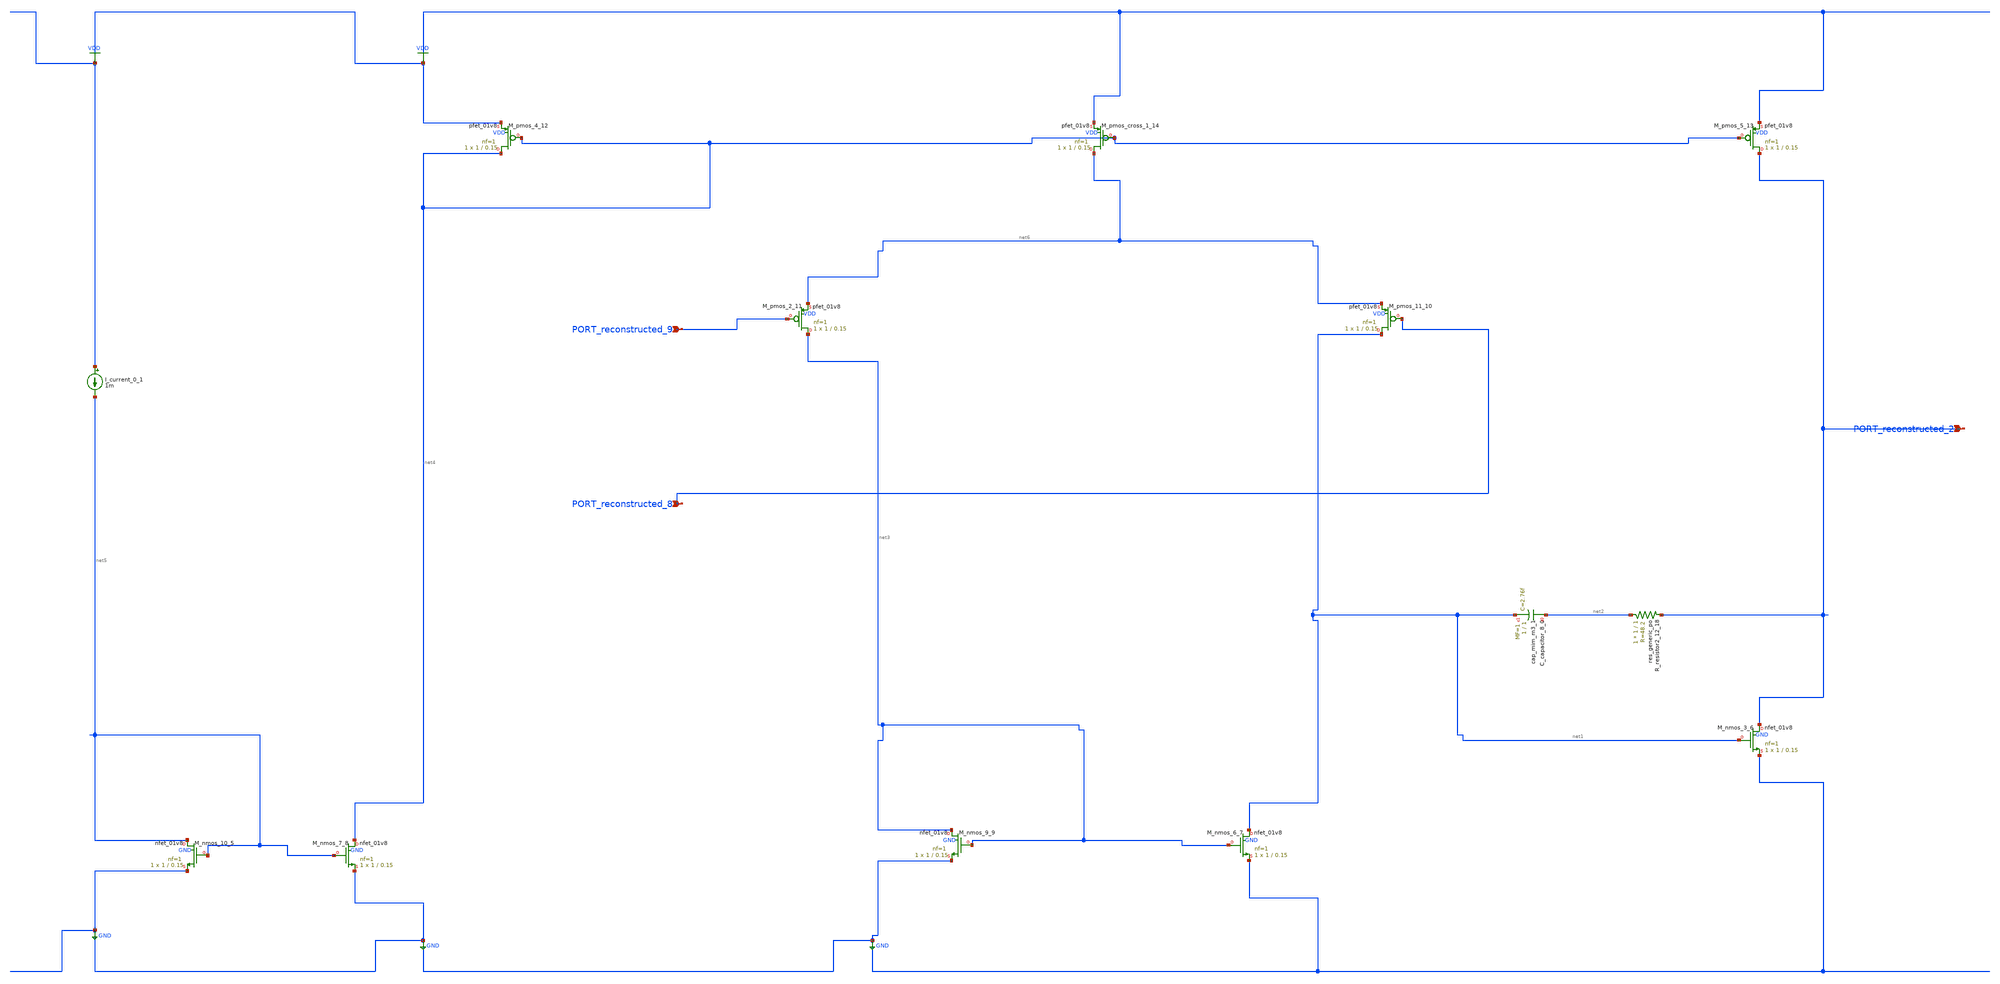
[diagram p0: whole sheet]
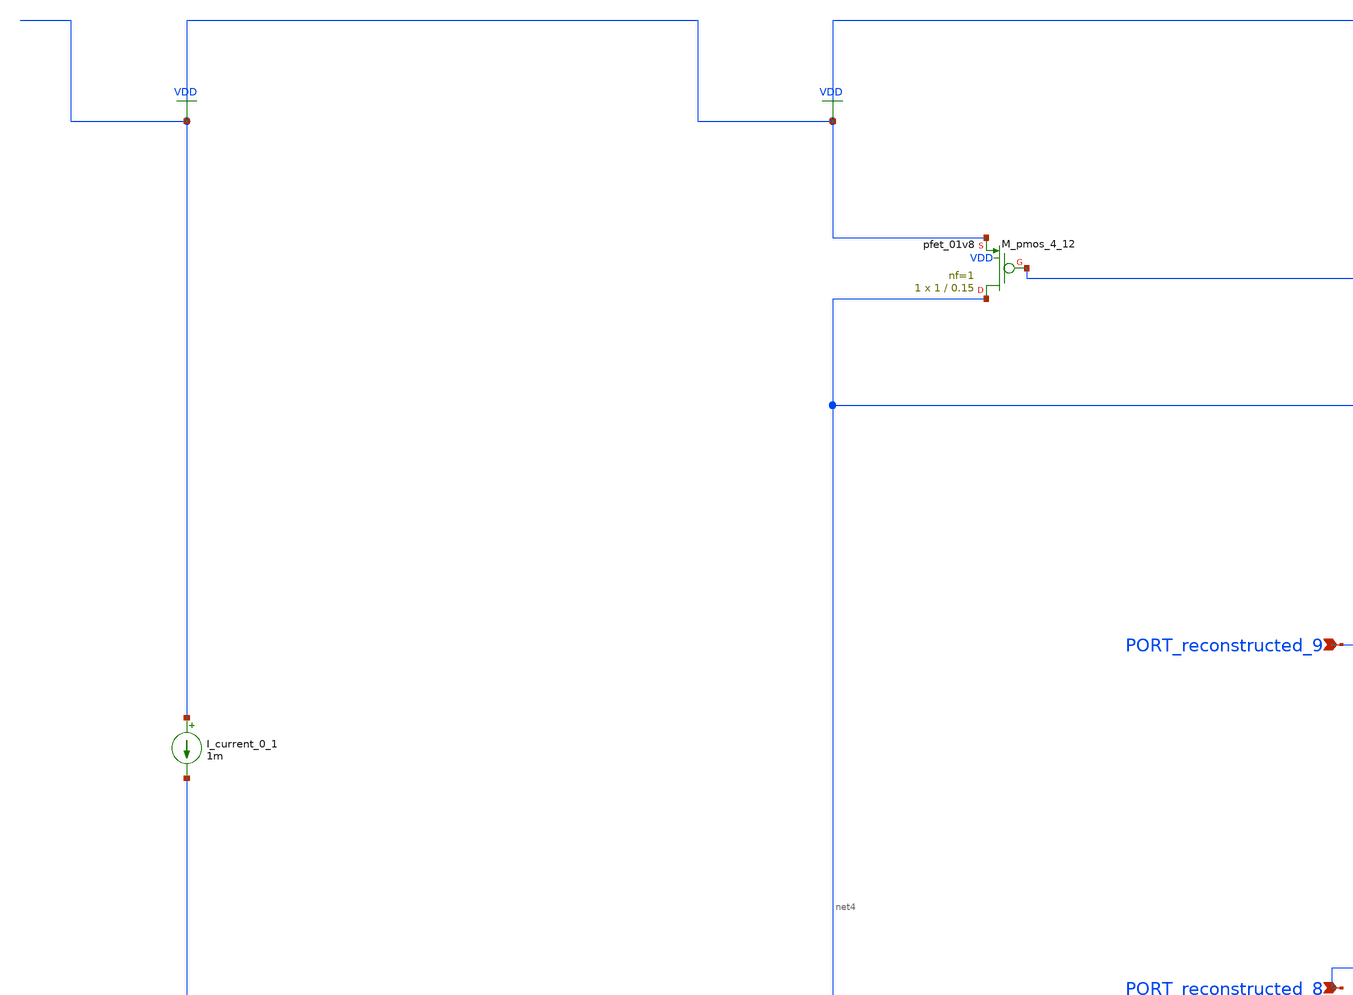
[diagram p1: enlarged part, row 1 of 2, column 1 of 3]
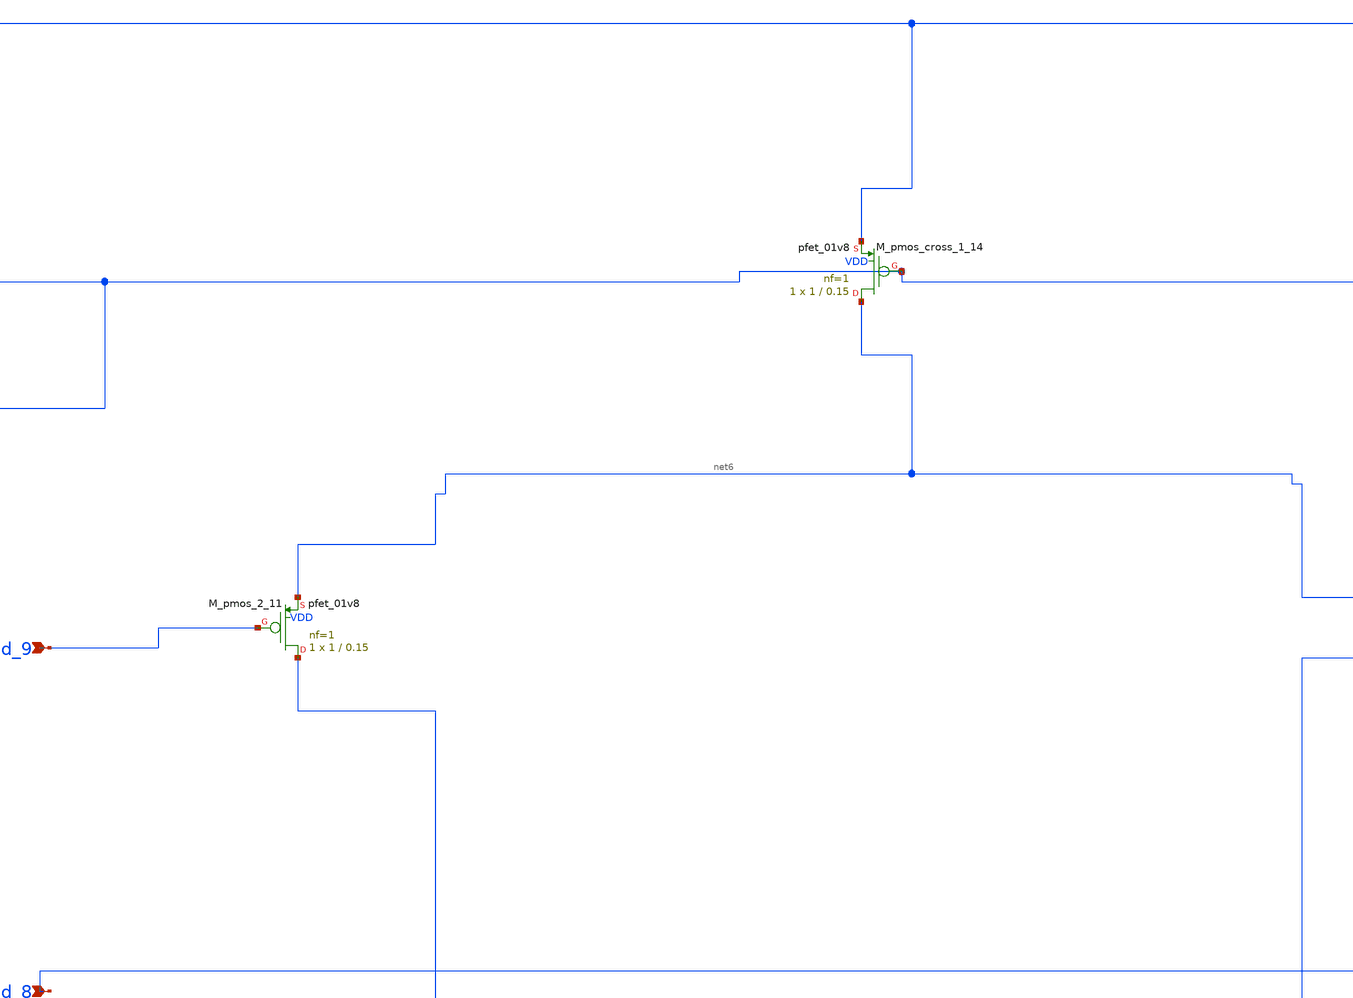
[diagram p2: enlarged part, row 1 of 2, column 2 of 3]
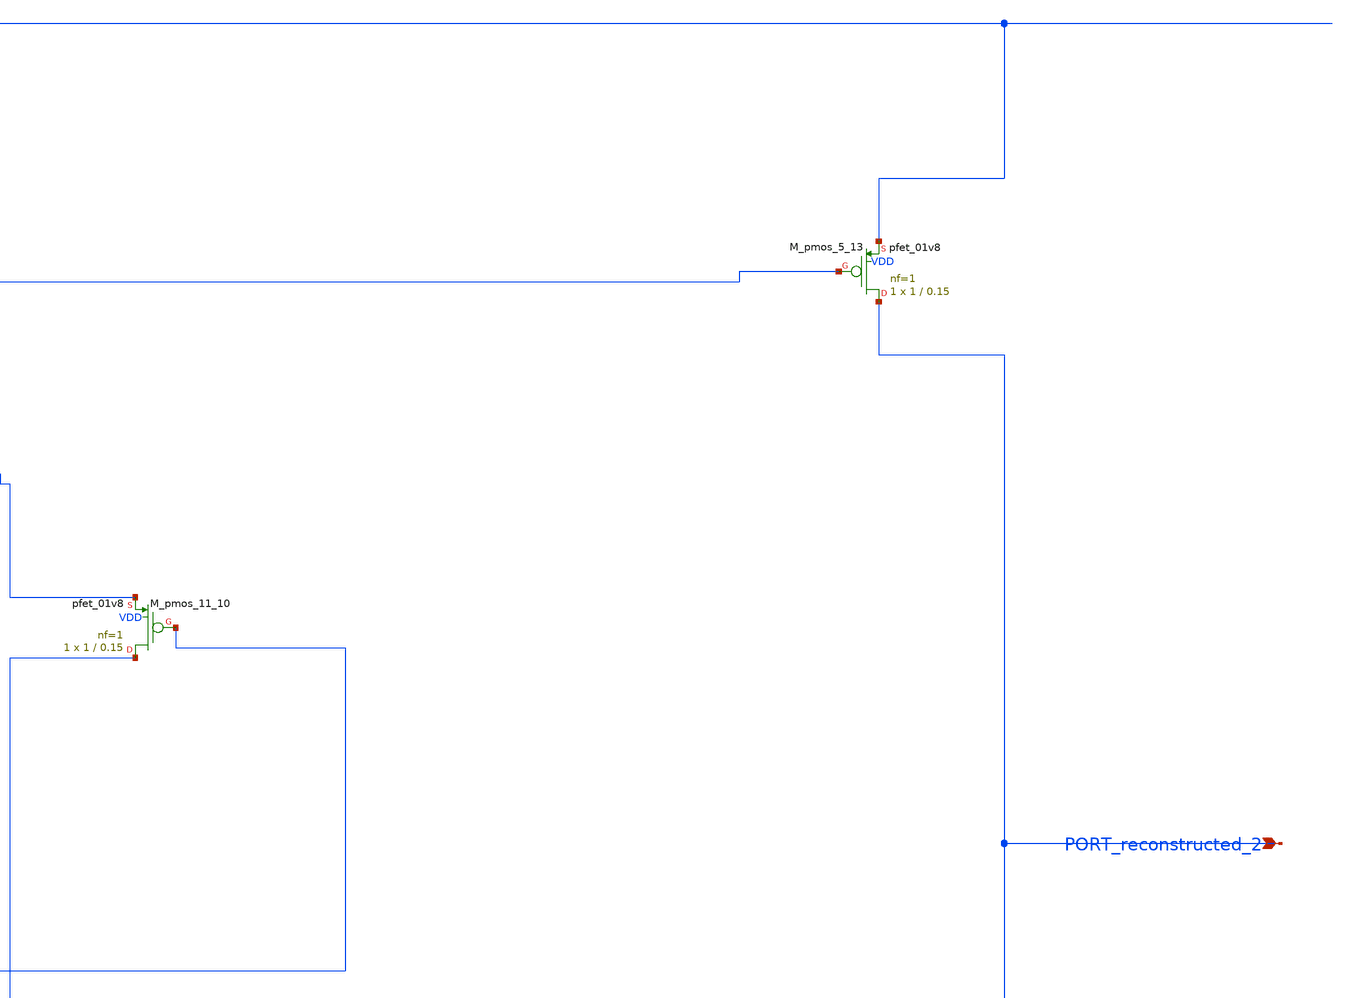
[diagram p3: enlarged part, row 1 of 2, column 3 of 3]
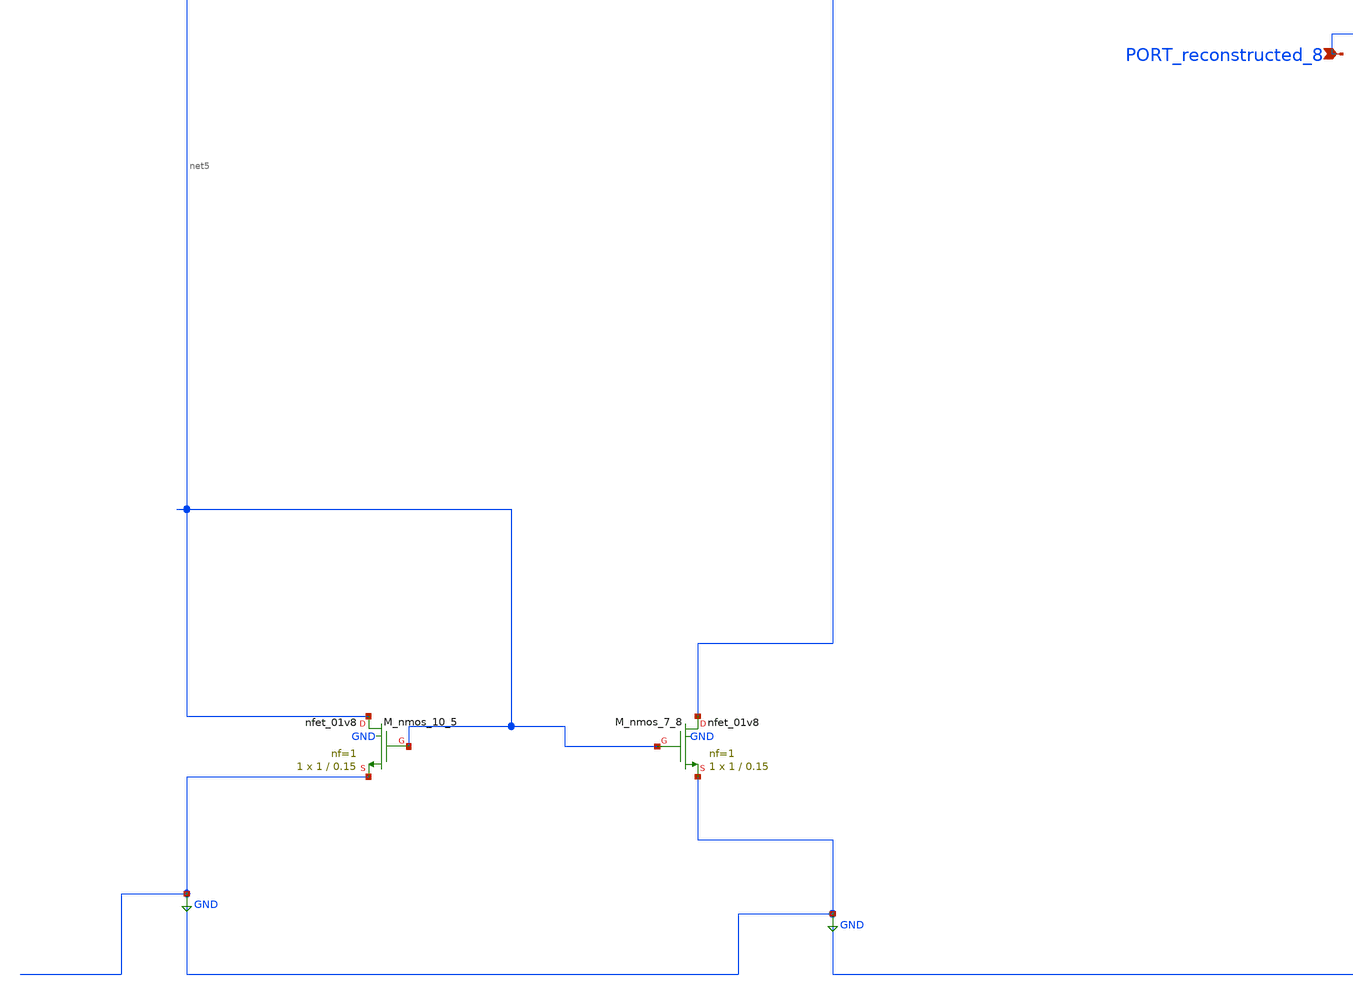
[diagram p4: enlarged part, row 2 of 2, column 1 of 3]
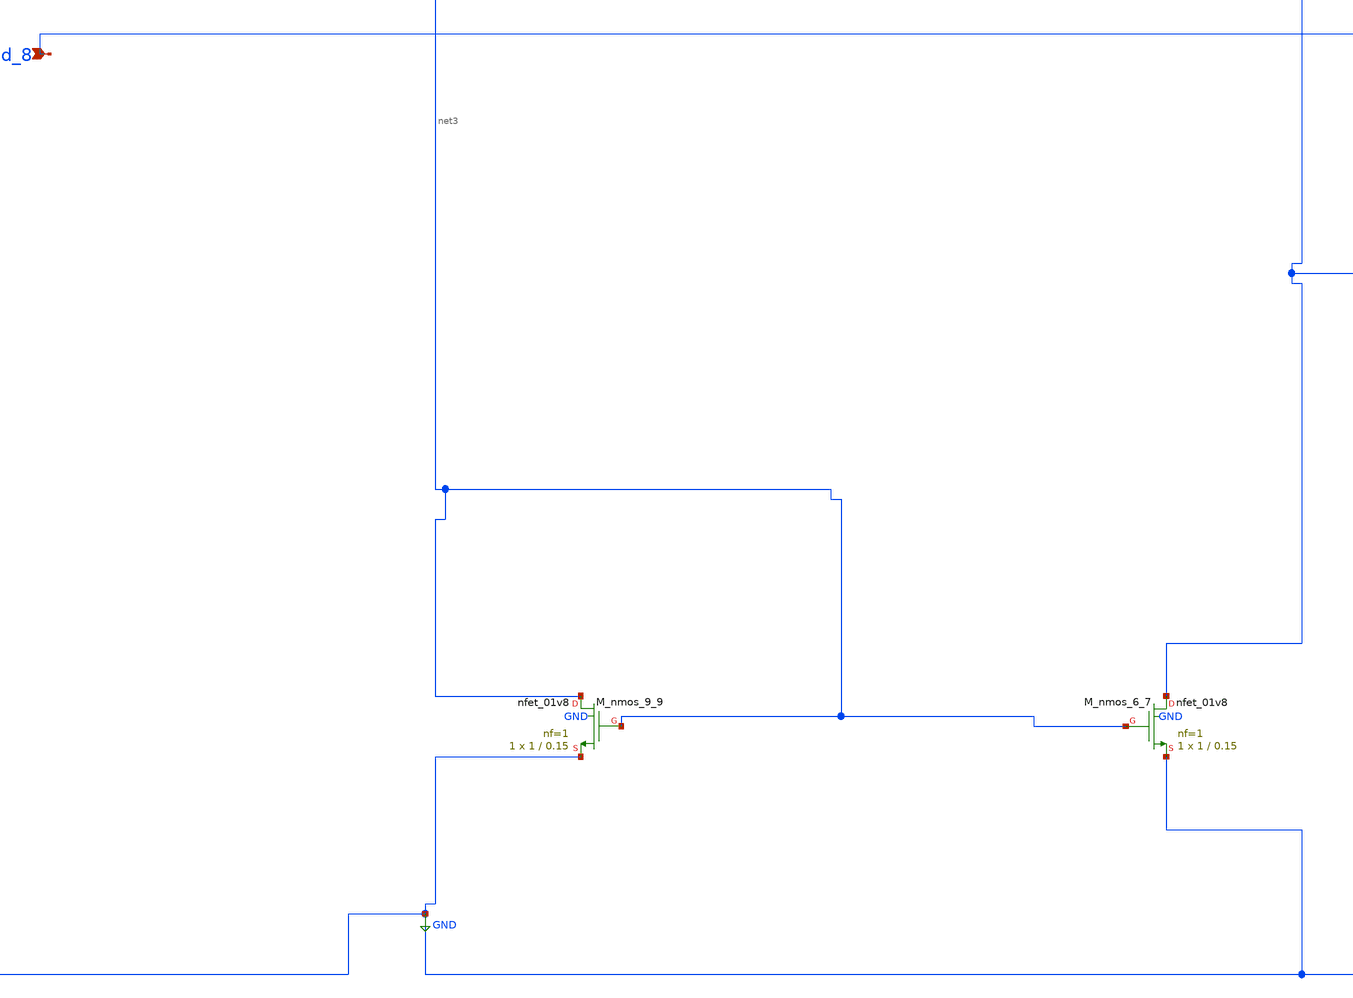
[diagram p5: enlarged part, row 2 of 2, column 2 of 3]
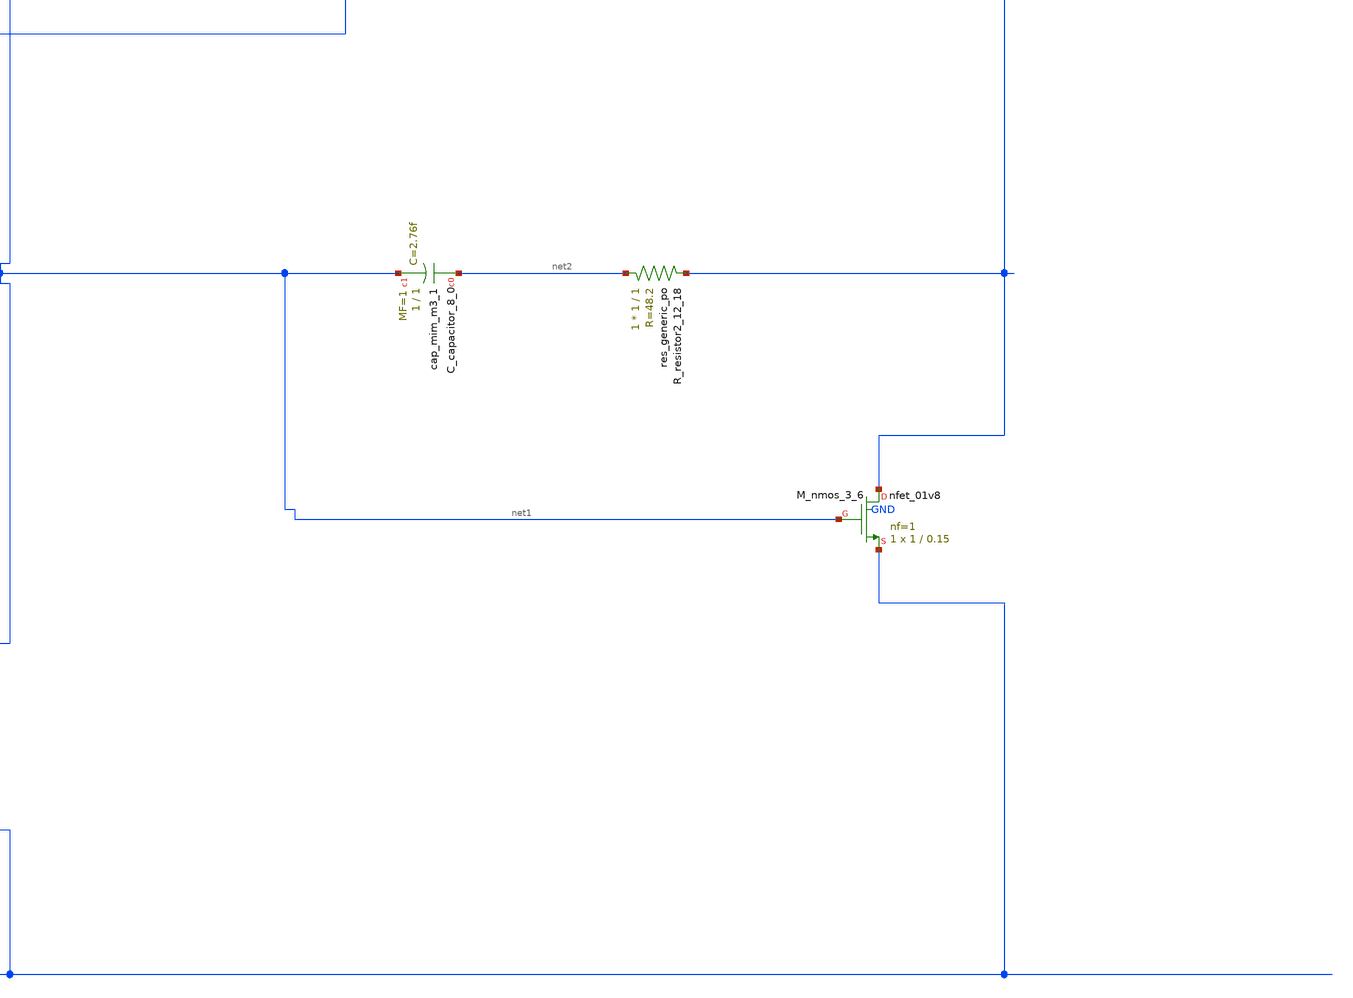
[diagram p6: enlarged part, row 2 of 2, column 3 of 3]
** sch_path: schematics/Image2Net/119.sch
**.subckt 119 PORT_reconstructed_2 PORT_reconstructed_8 PORT_reconstructed_9
*.ipin PORT_reconstructed_2
*.ipin PORT_reconstructed_8
*.ipin PORT_reconstructed_9
XC_capacitor_8_0 net2 net1 sky130_fd_pr__cap_mim_m3_1 W=1 L=1 MF=1 m=1
I_current_0_1 VDD net5 1m
XM_nmos_10_5 net5 net5 GND GND sky130_fd_pr__nfet_01v8 L=0.15 W=1 nf=1 ad='int((1 + 1)/2) * 1 / 1 * 0.29'
+ as='int((1 + 2)/2) * 1 / 1 * 0.29' pd='2*int((1 + 1)/2) * (1 / 1 + 0.29)' ps='2*int((1 + 2)/2) * (1 / 1 + 0.29)'
+ nrd='0.29 / 1 ' nrs='0.29 / 1 ' sa=0 sb=0 sd=0 mult=1 m=1
XM_nmos_3_6 PORT_reconstructed_2 net1 GND GND sky130_fd_pr__nfet_01v8 L=0.15 W=1 nf=1 ad='int((1 + 1)/2) * 1 / 1 * 0.29'
+ as='int((1 + 2)/2) * 1 / 1 * 0.29' pd='2*int((1 + 1)/2) * (1 / 1 + 0.29)' ps='2*int((1 + 2)/2) * (1 / 1 + 0.29)'
+ nrd='0.29 / 1 ' nrs='0.29 / 1 ' sa=0 sb=0 sd=0 mult=1 m=1
XM_nmos_6_7 net1 net3 GND GND sky130_fd_pr__nfet_01v8 L=0.15 W=1 nf=1 ad='int((1 + 1)/2) * 1 / 1 * 0.29'
+ as='int((1 + 2)/2) * 1 / 1 * 0.29' pd='2*int((1 + 1)/2) * (1 / 1 + 0.29)' ps='2*int((1 + 2)/2) * (1 / 1 + 0.29)'
+ nrd='0.29 / 1 ' nrs='0.29 / 1 ' sa=0 sb=0 sd=0 mult=1 m=1
XM_nmos_7_8 net4 net5 GND GND sky130_fd_pr__nfet_01v8 L=0.15 W=1 nf=1 ad='int((1 + 1)/2) * 1 / 1 * 0.29'
+ as='int((1 + 2)/2) * 1 / 1 * 0.29' pd='2*int((1 + 1)/2) * (1 / 1 + 0.29)' ps='2*int((1 + 2)/2) * (1 / 1 + 0.29)'
+ nrd='0.29 / 1 ' nrs='0.29 / 1 ' sa=0 sb=0 sd=0 mult=1 m=1
XM_nmos_9_9 net3 net3 GND GND sky130_fd_pr__nfet_01v8 L=0.15 W=1 nf=1 ad='int((1 + 1)/2) * 1 / 1 * 0.29'
+ as='int((1 + 2)/2) * 1 / 1 * 0.29' pd='2*int((1 + 1)/2) * (1 / 1 + 0.29)' ps='2*int((1 + 2)/2) * (1 / 1 + 0.29)'
+ nrd='0.29 / 1 ' nrs='0.29 / 1 ' sa=0 sb=0 sd=0 mult=1 m=1
XM_pmos_11_10 net1 PORT_reconstructed_8 net6 VDD sky130_fd_pr__pfet_01v8 L=0.15 W=1 nf=1 ad='int((1 + 1)/2) * 1 / 1 * 0.29'
+ as='int((1 + 2)/2) * 1 / 1 * 0.29' pd='2*int((1 + 1)/2) * (1 / 1 + 0.29)' ps='2*int((1 + 2)/2) * (1 / 1 + 0.29)'
+ nrd='0.29 / 1 ' nrs='0.29 / 1 ' sa=0 sb=0 sd=0 mult=1 m=1
XM_pmos_2_11 net3 PORT_reconstructed_9 net6 VDD sky130_fd_pr__pfet_01v8 L=0.15 W=1 nf=1 ad='int((1 + 1)/2) * 1 / 1 * 0.29'
+ as='int((1 + 2)/2) * 1 / 1 * 0.29' pd='2*int((1 + 1)/2) * (1 / 1 + 0.29)' ps='2*int((1 + 2)/2) * (1 / 1 + 0.29)'
+ nrd='0.29 / 1 ' nrs='0.29 / 1 ' sa=0 sb=0 sd=0 mult=1 m=1
XM_pmos_4_12 net4 net4 VDD VDD sky130_fd_pr__pfet_01v8 L=0.15 W=1 nf=1 ad='int((1 + 1)/2) * 1 / 1 * 0.29'
+ as='int((1 + 2)/2) * 1 / 1 * 0.29' pd='2*int((1 + 1)/2) * (1 / 1 + 0.29)' ps='2*int((1 + 2)/2) * (1 / 1 + 0.29)'
+ nrd='0.29 / 1 ' nrs='0.29 / 1 ' sa=0 sb=0 sd=0 mult=1 m=1
XM_pmos_5_13 PORT_reconstructed_2 net4 VDD VDD sky130_fd_pr__pfet_01v8 L=0.15 W=1 nf=1 ad='int((1 + 1)/2) * 1 / 1 * 0.29'
+ as='int((1 + 2)/2) * 1 / 1 * 0.29' pd='2*int((1 + 1)/2) * (1 / 1 + 0.29)' ps='2*int((1 + 2)/2) * (1 / 1 + 0.29)'
+ nrd='0.29 / 1 ' nrs='0.29 / 1 ' sa=0 sb=0 sd=0 mult=1 m=1
XM_pmos_cross_1_14 net6 net4 VDD VDD sky130_fd_pr__pfet_01v8 L=0.15 W=1 nf=1 ad='int((1 + 1)/2) * 1 / 1 * 0.29'
+ as='int((1 + 2)/2) * 1 / 1 * 0.29' pd='2*int((1 + 1)/2) * (1 / 1 + 0.29)' ps='2*int((1 + 2)/2) * (1 / 1 + 0.29)'
+ nrd='0.29 / 1 ' nrs='0.29 / 1 ' sa=0 sb=0 sd=0 mult=1 m=1
XR_resistor2_12_18 net2 PORT_reconstructed_2 sky130_fd_pr__res_generic_po W=1 L=1 m=1
**.ends
.GLOBAL GND
.GLOBAL VDD
.end
